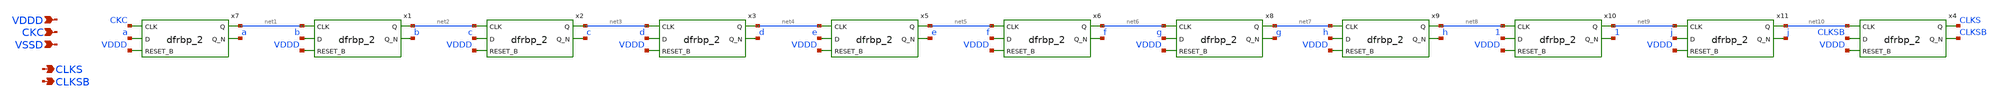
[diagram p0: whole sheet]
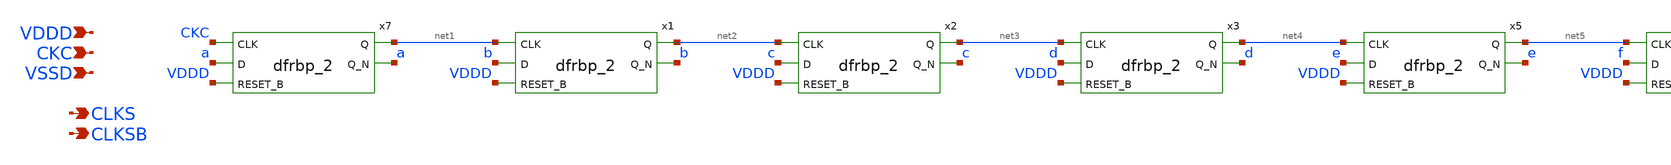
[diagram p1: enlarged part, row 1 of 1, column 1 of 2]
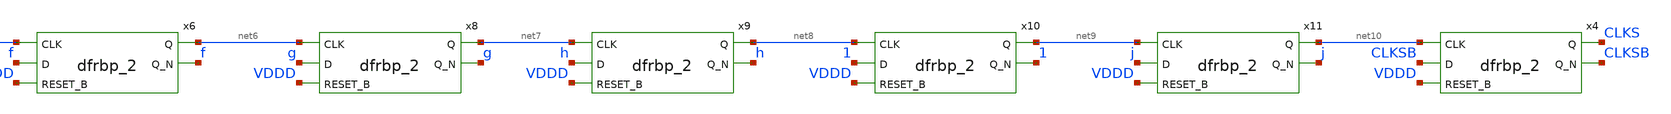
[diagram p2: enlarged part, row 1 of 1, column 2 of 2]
** sch_path: xschem/auto_sampling.sch
**.subckt auto_sampling CKC VDDD VSSD CLKS CLKSB
*.ipin CKC
*.ipin VDDD
*.ipin VSSD
*.opin CLKS
*.opin CLKSB
x7 CKC a VDDD VSSD VSSD VDDD VDDD net1 a sky130_fd_sc_hd__dfrbp_2
x1 net1 b VDDD VSSD VSSD VDDD VDDD net2 b sky130_fd_sc_hd__dfrbp_2
x2 net2 c VDDD VSSD VSSD VDDD VDDD net3 c sky130_fd_sc_hd__dfrbp_2
x4 net10 CLKSB VDDD VSSD VSSD VDDD VDDD CLKS CLKSB sky130_fd_sc_hd__dfrbp_2
x3 net3 d VDDD VSSD VSSD VDDD VDDD net4 d sky130_fd_sc_hd__dfrbp_2
x5 net4 e VDDD VSSD VSSD VDDD VDDD net5 e sky130_fd_sc_hd__dfrbp_2
x6 net5 f VDDD VSSD VSSD VDDD VDDD net6 f sky130_fd_sc_hd__dfrbp_2
x8 net6 g VDDD VSSD VSSD VDDD VDDD net7 g sky130_fd_sc_hd__dfrbp_2
x9 net7 h VDDD VSSD VSSD VDDD VDDD net8 h sky130_fd_sc_hd__dfrbp_2
x10 net8 1 VDDD VSSD VSSD VDDD VDDD net9 1 sky130_fd_sc_hd__dfrbp_2
x11 net9 j VDDD VSSD VSSD VDDD VDDD net10 j sky130_fd_sc_hd__dfrbp_2
**.ends
.end
